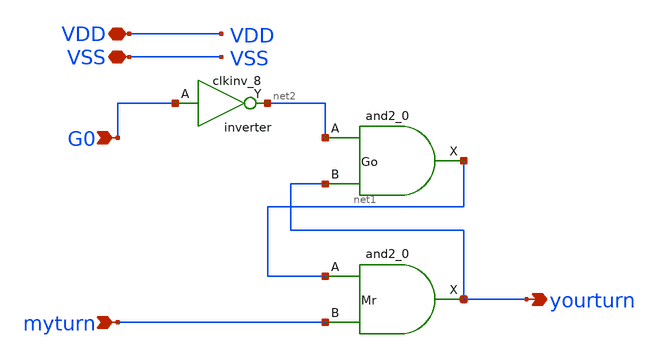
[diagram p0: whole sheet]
** sch_path: xschem/base-joint.sch
**.subckt base-joint G0 myturn yourturn VDD VSS
*.ipin G0
*.ipin myturn
*.opin yourturn
*.iopin VDD
*.iopin VSS
Mr net1 myturn VSS VSS VDD VDD yourturn sky130_fd_sc_hd__and2_0
Go net2 yourturn VSS VSS VDD VDD net1 sky130_fd_sc_hd__and2_0
inverter G0 VSS VSS VDD VDD net2 sky130_fd_sc_hd__clkinv_8
**.ends
.end
